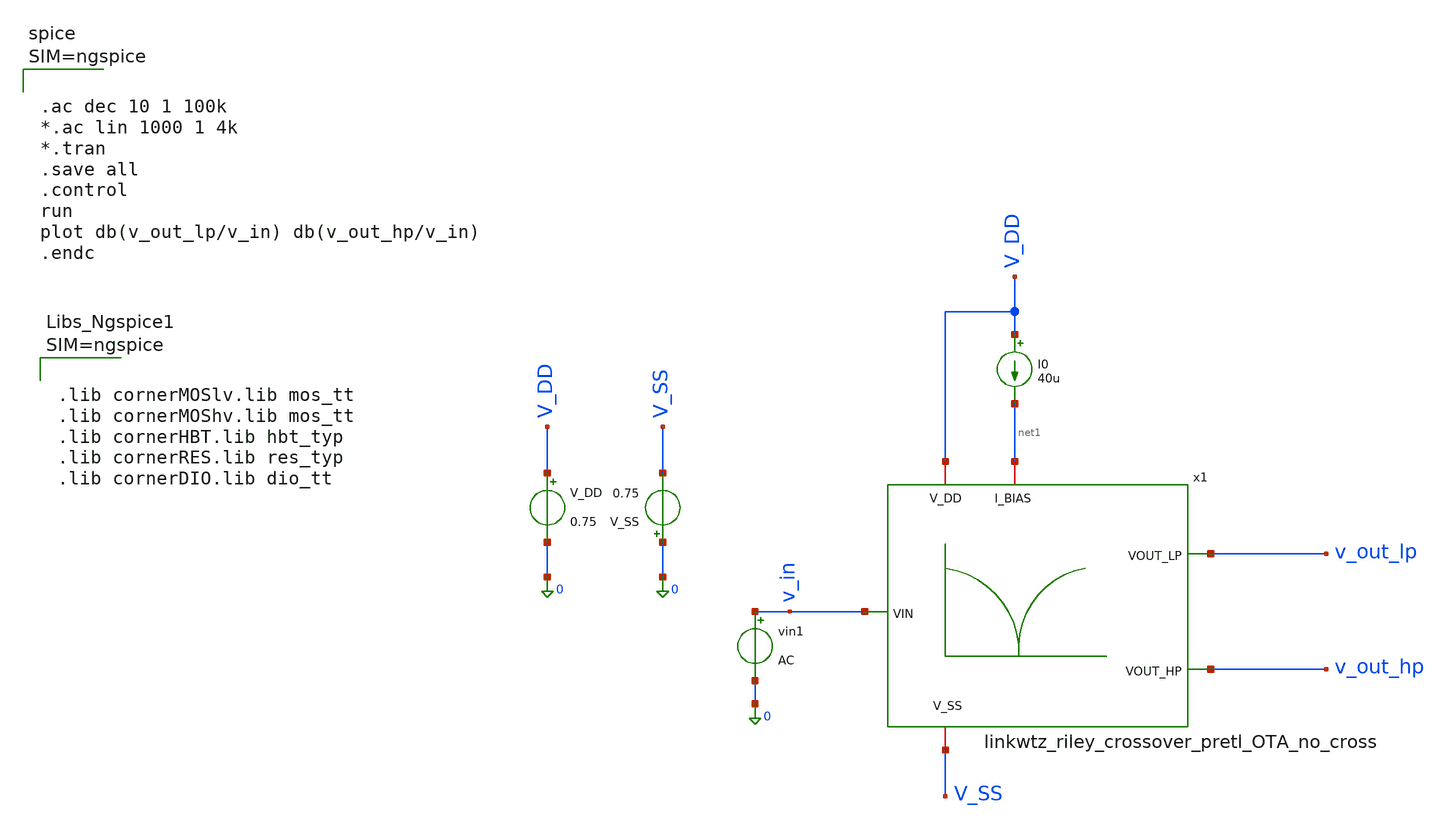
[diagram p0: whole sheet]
** sch_path: 004_Real_Circuits/001_version_basic_ota_pretl/linkwitz_riley_real_circuit_pretl_no_cross_top_tb.sch
* 004_Real_Circuits/001_version_basic_ota_pretl/ota-5t.sch:
* (c) 2024-2025 Harald Pretl, Apache-2.0 license
**.subckt linkwitz_riley_real_circuit_pretl_no_cross_top_tb
I0 V_DD net1 40u
vin1 v_in 0 AC
x1 v_out_lp net1 V_DD V_SS v_in v_out_hp linkwtz_riley_crossover_pretl_OTA_no_cross
V_DD V_DD 0 0.75
V_SS 0 V_SS 0.75
**** begin user architecture code



.lib cornerMOSlv.lib mos_tt
.lib cornerMOShv.lib mos_tt
.lib cornerHBT.lib hbt_typ
.lib cornerRES.lib res_typ
.lib cornerDIO.lib dio_tt






.ac dec 10 1 100k
*.ac lin 1000 1 4k
*.tran
.save all
.control
run
plot db(v_out_lp/v_in) db(v_out_hp/v_in)
.endc



**** end user architecture code
**.ends

* expanding   symbol:
*+  004_Real_Circuits/001_version_basic_ota_pretl/linkwtz_riley_crossover_pretl_OTA_no_cross.sym # of pins=6
** sym_path: 004_Real_Circuits/001_version_basic_ota_pretl/linkwtz_riley_crossover_pretl_OTA_no_cross.sym
** sch_path: 004_Real_Circuits/001_version_basic_ota_pretl/linkwtz_riley_crossover_pretl_OTA_no_cross.sch
.subckt linkwtz_riley_crossover_pretl_OTA_no_cross VOUT_LP I_BIAS V_DD V_SS VIN VOUT_HP
*.opin VOUT_LP
*.opin VOUT_HP
*.ipin VIN
*.iopin I_BIAS
*.iopin V_DD
*.iopin V_SS
R1 net1 VIN R_LP m=1
R2 net2 net1 R_LP m=1
C1 net2 0 C_LP m=1
C2 net1 VOUT_LP C_LP m=1
C3 VIN net3 C_HP m=1
C4 net3 net4 C_HP m=1
R3 net3 VOUT_HP R_HP m=1
R4 net4 0 R_HP m=1
x1 V_DD VOUT_LP net2 VOUT_LP I_BIAS V_DD V_SS ota-5t
x2 V_DD VOUT_HP net4 VOUT_HP I_BIAS V_DD V_SS ota-5t
.param C_LP=1.06e-8
.param R_LP=100k
.param C_HP=50e-10
.param R_HP=212.20k
.param R_IN=100k
.ends


* expanding   symbol:  004_Real_Circuits/001_version_basic_ota_pretl/ota-5t.sym # of pins=7
** sym_path: 004_Real_Circuits/001_version_basic_ota_pretl/ota-5t.sym
** sch_path: 004_Real_Circuits/001_version_basic_ota_pretl/ota-5t.sch
.subckt ota-5t vdd vout vinp vinn ibias_20u d_ena vss
*.ipin ibias_20u
*.iopin vdd
*.iopin vss
*.ipin vinp
*.ipin vinn
*.opin vout
*.ipin d_ena
XM5 tail gate_n vss vss sg13_lv_nmos w=1.5u l=5u ng=1 m=1 mm_ok=1
XM4 vout gate_p vdd vdd sg13_lv_pmos w=3.5u l=5u ng=1 m=1 mm_ok=1
XM1 gate_p vinp tail vss sg13_lv_nmos w=2u l=5u ng=1 m=1 mm_ok=1
XM2 vout vinn tail vss sg13_lv_nmos w=2u l=5u ng=1 m=1 mm_ok=1
XM3 gate_p gate_p vdd vdd sg13_lv_pmos w=3.5u l=5u ng=1 m=1 mm_ok=1
XM6 ibias_20u gate_n vss vss sg13_lv_nmos w=10u l=5u ng=5 m=1 mm_ok=1
XM9 gate_n ena_n vss vss sg13_lv_nmos w=0.5u l=0.13u ng=1 m=1 mm_ok=1
XM11 gate_p ena vdd vdd sg13_lv_pmos w=1.5u l=0.13u ng=1 m=1 mm_ok=1
XM7 ena ena_n vss vss sg13_lv_nmos w=0.5u l=0.13u ng=1 m=1 mm_ok=1
XM8 ena ena_n vdd vdd sg13_lv_pmos w=1.5u l=0.13u ng=1 m=1 mm_ok=1
XM10 ibias_20u ena gate_n vss sg13_lv_nmos w=0.5u l=0.13u ng=1 m=1 mm_ok=1
XM12 ena_n d_ena vss vss sg13_lv_nmos w=0.5u l=0.13u ng=1 m=1 mm_ok=1
XM13 ena_n d_ena vdd vdd sg13_lv_pmos w=1.5u l=0.13u ng=1 m=1 mm_ok=1
.ends

.end
